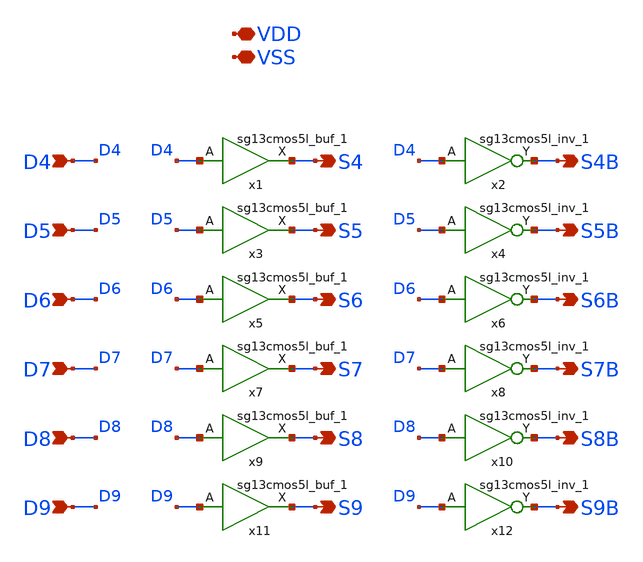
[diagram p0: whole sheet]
** sch_path: designs/libs/core_digital/fine_driver_6b/fine_driver_6b.sch
**.subckt fine_driver_6b D4 S4 S4B VDD VSS D5 S5 S5B D6 S6 S6B D7 S7 S7B D8 S8 S8B D9 S9 S9B
*.ipin D4
*.opin S4
*.opin S4B
*.iopin VDD
*.iopin VSS
*.ipin D5
*.opin S5
*.opin S5B
*.ipin D6
*.opin S6
*.opin S6B
*.ipin D7
*.opin S7
*.opin S7B
*.ipin D8
*.opin S8
*.opin S8B
*.ipin D9
*.opin S9
*.opin S9B
x1 S4 D4 VDD VSS sg13cmos5l_buf_1
x2 S4B D4 VDD VSS sg13cmos5l_inv_1
x3 S5 D5 VDD VSS sg13cmos5l_buf_1
x4 S5B D5 VDD VSS sg13cmos5l_inv_1
x5 S6 D6 VDD VSS sg13cmos5l_buf_1
x6 S6B D6 VDD VSS sg13cmos5l_inv_1
x7 S7 D7 VDD VSS sg13cmos5l_buf_1
x8 S7B D7 VDD VSS sg13cmos5l_inv_1
x9 S8 D8 VDD VSS sg13cmos5l_buf_1
x10 S8B D8 VDD VSS sg13cmos5l_inv_1
x11 S9 D9 VDD VSS sg13cmos5l_buf_1
x12 S9B D9 VDD VSS sg13cmos5l_inv_1
**.ends
.end
